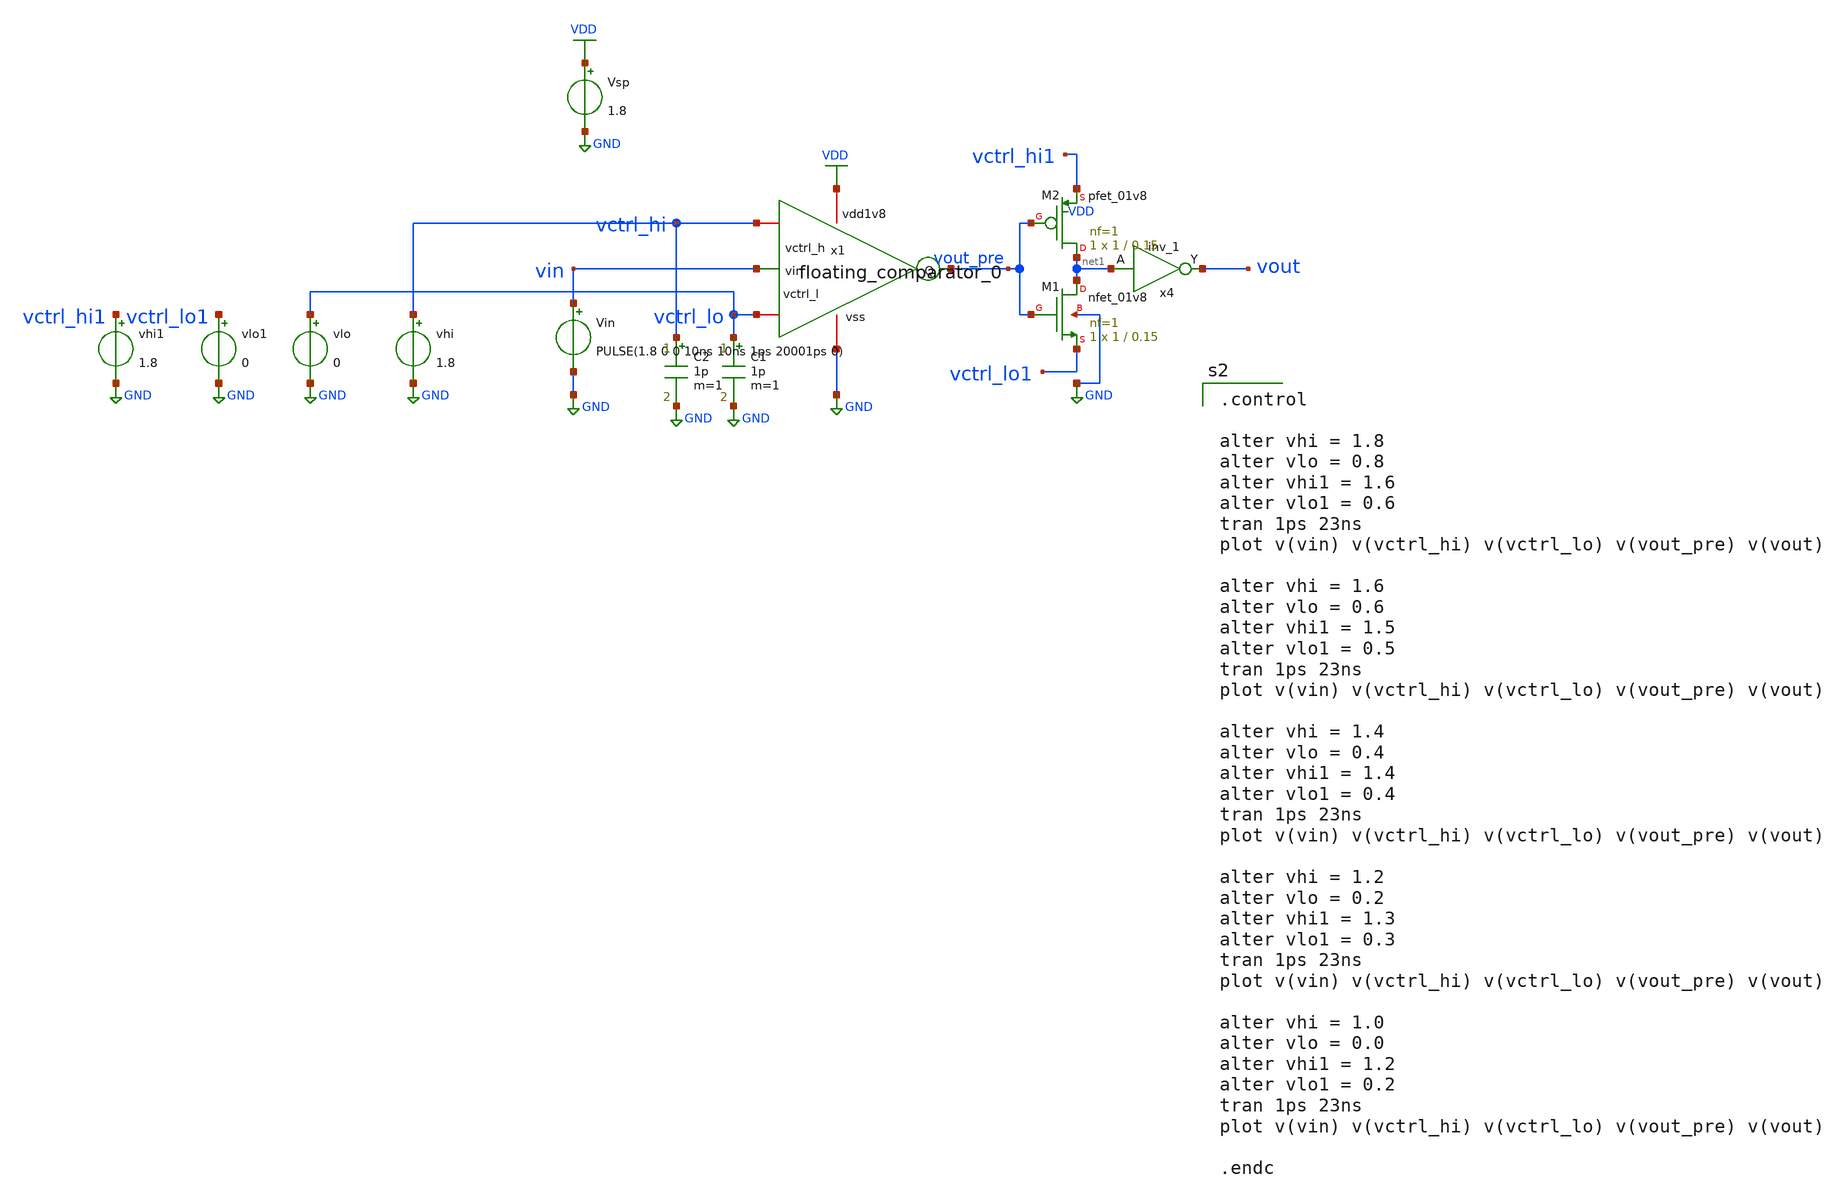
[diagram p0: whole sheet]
** sch_path: xschem/floating_comparator_tb.sch
**.subckt floating_comparator_tb
x1 VDD vctrl_hi vout_pre vin GND vctrl_lo floating_comparator_0
Vsp VDD GND 1.8
Vin vin GND PULSE(1.8 0 0 10ns 10ns 1ps 20001ps 0)
C1 vctrl_lo GND 1p m=1
C2 vctrl_hi GND 1p m=1
vhi vctrl_hi GND 1.8
vlo vctrl_lo GND 0
x4 net1 GND GND VDD VDD vout sky130_fd_sc_hvl__inv_1
vhi1 vctrl_hi1 GND 1.8
vlo1 vctrl_lo1 GND 0
XM1 net1 vout_pre vctrl_lo1 GND sky130_fd_pr__nfet_01v8 L=0.15 W=1 nf=1 ad='int((nf+1)/2) * W/nf * 0.29'
+ as='int((nf+2)/2) * W/nf * 0.29' pd='2*int((nf+1)/2) * (W/nf + 0.29)' ps='2*int((nf+2)/2) * (W/nf + 0.29)'
+ nrd='0.29 / W' nrs='0.29 / W' sa=0 sb=0 sd=0 mult=1 m=1
XM2 net1 vout_pre vctrl_hi1 VDD sky130_fd_pr__pfet_01v8 L=0.15 W=1 nf=1 ad='int((nf+1)/2) * W/nf * 0.29'
+ as='int((nf+2)/2) * W/nf * 0.29' pd='2*int((nf+1)/2) * (W/nf + 0.29)' ps='2*int((nf+2)/2) * (W/nf + 0.29)'
+ nrd='0.29 / W' nrs='0.29 / W' sa=0 sb=0 sd=0 mult=1 m=1
**** begin user architecture code
.lib $::SKYWATER_MODELS/sky130.lib.spice tt
.include $::PDKPATH/libs.ref/sky130_fd_sc_hvl/spice/sky130_fd_sc_hvl.spice

.control

alter vhi = 1.8
alter vlo = 0.8
alter vhi1 = 1.6
alter vlo1 = 0.6
tran 1ps 23ns
plot v(vin) v(vctrl_hi) v(vctrl_lo) v(vout_pre) v(vout)

alter vhi = 1.6
alter vlo = 0.6
alter vhi1 = 1.5
alter vlo1 = 0.5
tran 1ps 23ns
plot v(vin) v(vctrl_hi) v(vctrl_lo) v(vout_pre) v(vout)

alter vhi = 1.4
alter vlo = 0.4
alter vhi1 = 1.4
alter vlo1 = 0.4
tran 1ps 23ns
plot v(vin) v(vctrl_hi) v(vctrl_lo) v(vout_pre) v(vout)

alter vhi = 1.2
alter vlo = 0.2
alter vhi1 = 1.3
alter vlo1 = 0.3
tran 1ps 23ns
plot v(vin) v(vctrl_hi) v(vctrl_lo) v(vout_pre) v(vout)

alter vhi = 1.0
alter vlo = 0.0
alter vhi1 = 1.2
alter vlo1 = 0.2
tran 1ps 23ns
plot v(vin) v(vctrl_hi) v(vctrl_lo) v(vout_pre) v(vout)

.endc


**** end user architecture code
**.ends

* expanding   symbol:  floating_comparator_0.sym # of pins=6
** sym_path: xschem/floating_comparator_0.sym
** sch_path: xschem/floating_comparator_0.sch
.subckt floating_comparator_0 vdd1v8 vctrl_h Q vin vss vctrl_l
*.iopin vdd1v8
*.iopin vss
*.opin Q
*.iopin vctrl_h
*.ipin vin
*.iopin vctrl_l
XM1 Q vin vctrl_l vss sky130_fd_pr__nfet_01v8 L=0.15 W=1 nf=1 ad='int((nf+1)/2) * W/nf * 0.29' as='int((nf+2)/2) * W/nf * 0.29'
+ pd='2*int((nf+1)/2) * (W/nf + 0.29)' ps='2*int((nf+2)/2) * (W/nf + 0.29)' nrd='0.29 / W' nrs='0.29 / W'
+ sa=0 sb=0 sd=0 mult=1 m=1
XM2 Q vin vctrl_h vdd1v8 sky130_fd_pr__pfet_01v8 L=0.15 W=2 nf=1 ad='int((nf+1)/2) * W/nf * 0.29' as='int((nf+2)/2) * W/nf * 0.29'
+ pd='2*int((nf+1)/2) * (W/nf + 0.29)' ps='2*int((nf+2)/2) * (W/nf + 0.29)' nrd='0.29 / W' nrs='0.29 / W'
+ sa=0 sb=0 sd=0 mult=1 m=1
.ends

.GLOBAL VDD
.GLOBAL GND
.end
